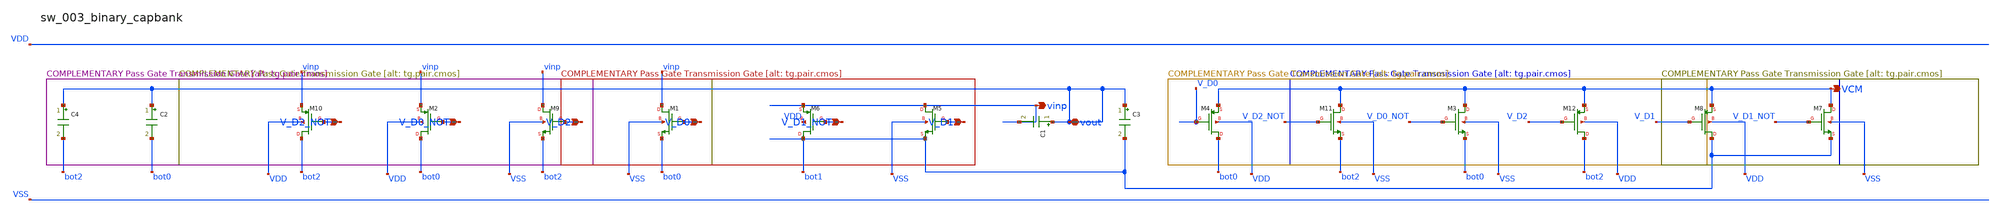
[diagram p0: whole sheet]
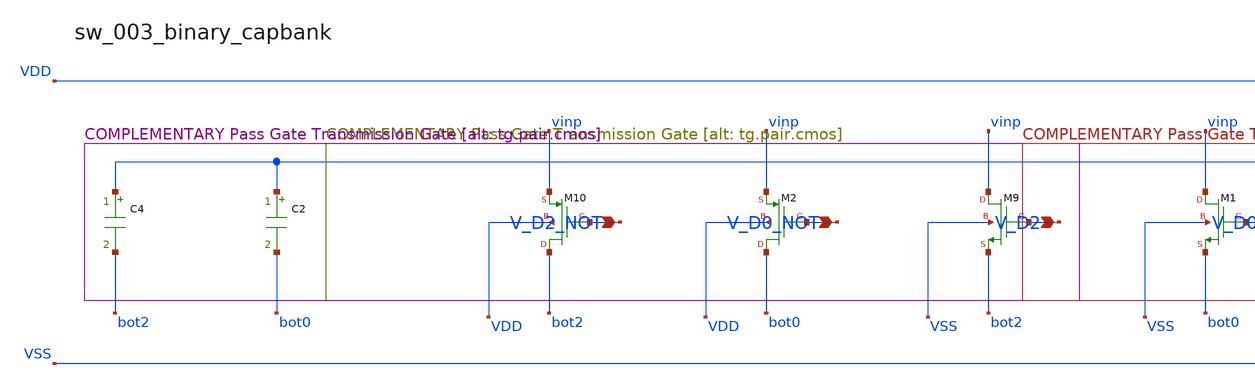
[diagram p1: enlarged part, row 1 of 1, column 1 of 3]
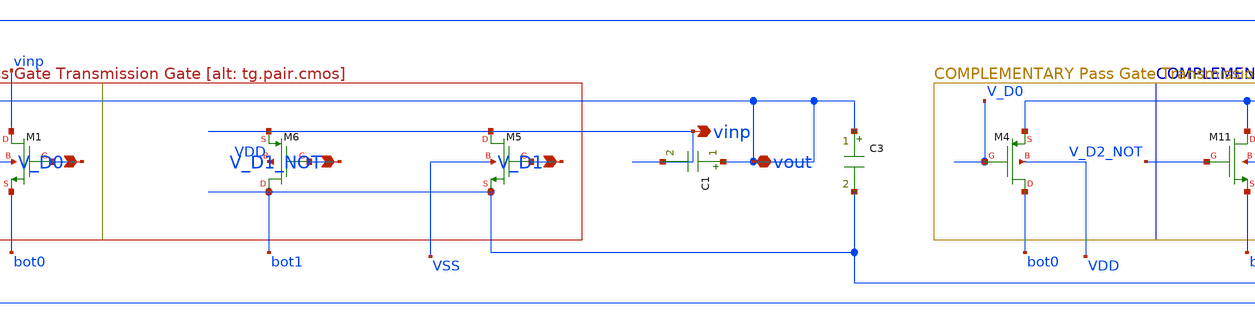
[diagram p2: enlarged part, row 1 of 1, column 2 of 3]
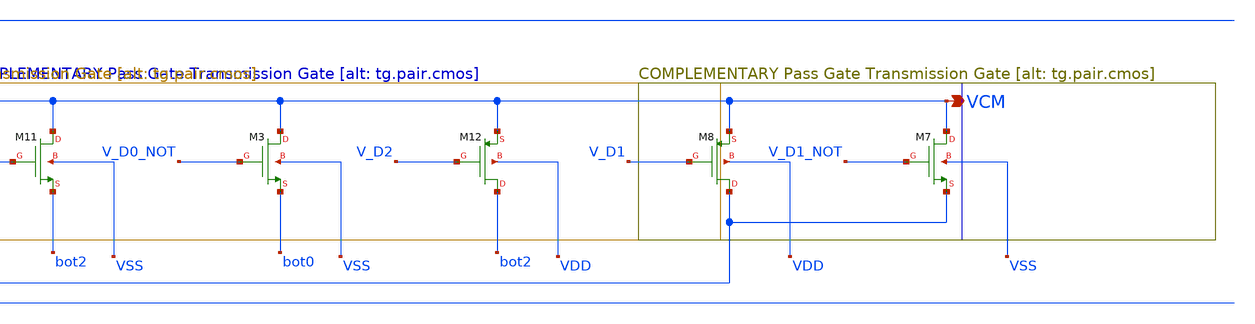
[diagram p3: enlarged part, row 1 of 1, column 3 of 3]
** sch_path: analog-db/raw/sw_003_binary_capbank/sw_003_binary_capbank_annotated.sch
**.subckt sw_003_binary_capbank_annotated V_D2_NOT V_D0_NOT V_D2 V_D0 V_D1_NOT V_D1 vout vinp VCM
*.ipin V_D2_NOT
*.ipin V_D0_NOT
*.ipin V_D2
*.ipin V_D0
*.ipin V_D1_NOT
*.ipin V_D1
*.iopin vout
*.opin vinp
*.opin VCM
C1 vout vinp 'Cu' m=x_dut_c1_m
C2 vout bot0 'Cu' m=x_dut_c2_m
C3 vout bot1 'Cu' m=x_dut_c3_m
C4 vout bot2 'Cu' m=x_dut_c4_m
XM1 vinp V_D0 bot0 VSS sg13_lv_nmos w=x_dut_xm1_w l=x_dut_xm1_l ng=1 m=x_dut_xm1_m
XM10 bot2 V_D2_NOT vinp VDD sg13_lv_pmos w=x_dut_xm10_w l=x_dut_xm10_l ng=1 m=x_dut_xm10_m
XM11 VCM V_D2_NOT bot2 VSS sg13_lv_nmos w=x_dut_xm11_w l=x_dut_xm11_l ng=1 m=x_dut_xm11_m
XM12 bot2 V_D2 VCM VDD sg13_lv_pmos w=x_dut_xm12_w l=x_dut_xm12_l ng=1 m=x_dut_xm12_m
XM2 bot0 V_D0_NOT vinp VDD sg13_lv_pmos w=x_dut_xm2_w l=x_dut_xm2_l ng=1 m=x_dut_xm2_m
XM3 VCM V_D0_NOT bot0 VSS sg13_lv_nmos w=x_dut_xm3_w l=x_dut_xm3_l ng=1 m=x_dut_xm3_m
XM4 bot0 V_D0 VCM VDD sg13_lv_pmos w=x_dut_xm4_w l=x_dut_xm4_l ng=1 m=x_dut_xm4_m
XM5 vinp V_D1 bot1 VSS sg13_lv_nmos w=x_dut_xm5_w l=x_dut_xm5_l ng=1 m=x_dut_xm5_m
XM6 bot1 V_D1_NOT vinp VDD sg13_lv_pmos w=x_dut_xm6_w l=x_dut_xm6_l ng=1 m=x_dut_xm6_m
XM7 VCM V_D1_NOT bot1 VSS sg13_lv_nmos w=x_dut_xm7_w l=x_dut_xm7_l ng=1 m=x_dut_xm7_m
XM8 bot1 V_D1 VCM VDD sg13_lv_pmos w=x_dut_xm8_w l=x_dut_xm8_l ng=1 m=x_dut_xm8_m
XM9 vinp V_D2 bot2 VSS sg13_lv_nmos w=x_dut_xm9_w l=x_dut_xm9_l ng=1 m=x_dut_xm9_m
**.ends
.end
